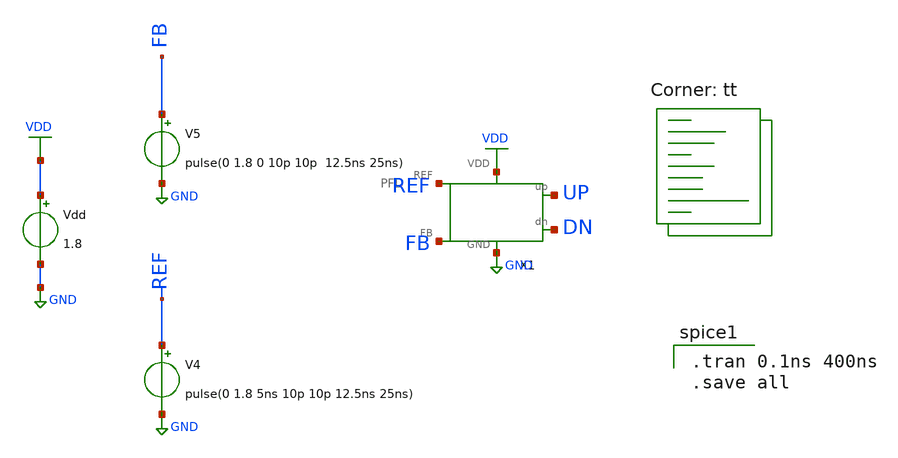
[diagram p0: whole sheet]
** sch_path: pll/pfd_cp_lf_lib/PFD_tb/xschem/PFD_tb.sch
**.subckt PFD_tb
X1 REF UP FB VDD GND DN PFD
Vdd VDD GND 1.8
V4 REF GND pulse(0 1.8 5ns 10p 10p 12.5ns 25ns)
V5 FB GND pulse(0 1.8 0 10p 10p 12.5ns 25ns)
**** begin user architecture code
.lib $::SKYWATER_MODELS/sky130.lib.spice tt

.tran 0.1ns 400ns
.save all

**** end user architecture code
**.ends
.GLOBAL GND
.GLOBAL VDD
.end
